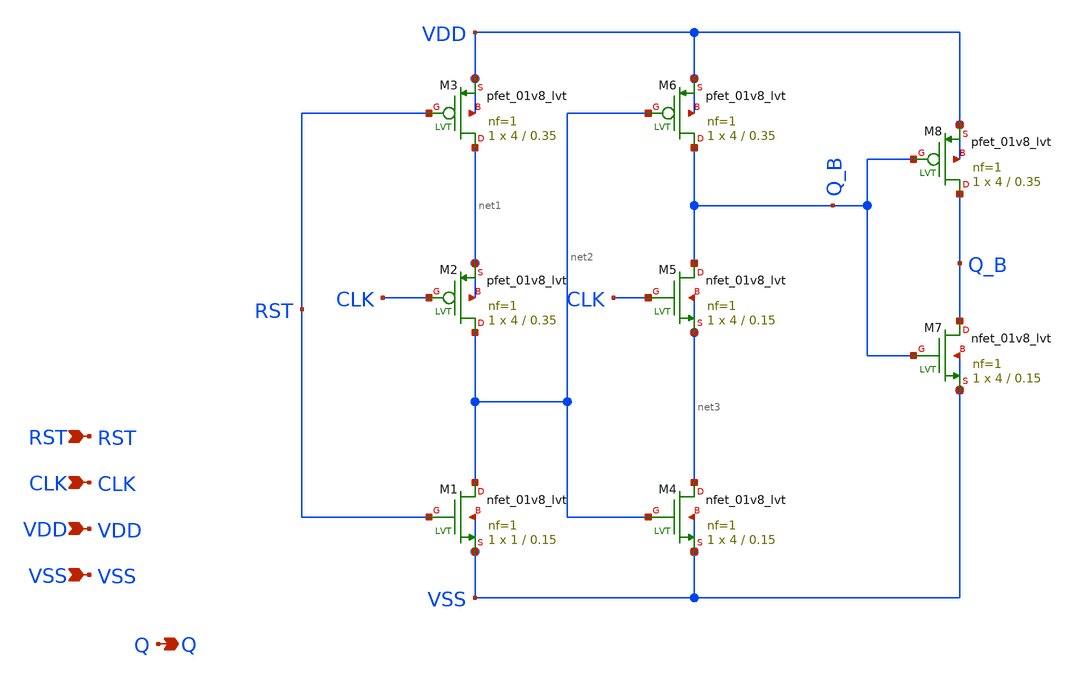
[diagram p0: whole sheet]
** sch_path: design/LELO_TSPC_FULL.sch
**.subckt LELO_TSPC_FULL RST CLK VDD VSS Q
*.ipin RST
*.ipin CLK
*.ipin VDD
*.ipin VSS
*.opin Q
XM1 net2 RST VSS VSS sky130_fd_pr__nfet_01v8_lvt L=0.15 W=1 nf=1 ad='int((1 + 1)/2) * 1 / 1 * 0.29' as='int((1 + 2)/2) * 1 / 1 * 0.29'
+ pd='2*int((1 + 1)/2) * (1 / 1 + 0.29)' ps='2*int((1 + 2)/2) * (1 / 1 + 0.29)' nrd='0.29 / 1 ' nrs='0.29 / 1 '
+ sa=0 sb=0 sd=0 mult=1 m=1
XM2 net2 CLK net1 net1 sky130_fd_pr__pfet_01v8_lvt L=0.35 W=4 nf=1 ad='int((1 + 1)/2) * 4 / 1 * 0.29'
+ as='int((1 + 2)/2) * 4 / 1 * 0.29' pd='2*int((1 + 1)/2) * (4 / 1 + 0.29)' ps='2*int((1 + 2)/2) * (4 / 1 + 0.29)'
+ nrd='0.29 / 4 ' nrs='0.29 / 4 ' sa=0 sb=0 sd=0 mult=1 m=1
XM3 net1 RST VDD VDD sky130_fd_pr__pfet_01v8_lvt L=0.35 W=4 nf=1 ad='int((1 + 1)/2) * 4 / 1 * 0.29' as='int((1 + 2)/2) * 4 / 1 * 0.29'
+ pd='2*int((1 + 1)/2) * (4 / 1 + 0.29)' ps='2*int((1 + 2)/2) * (4 / 1 + 0.29)' nrd='0.29 / 4 ' nrs='0.29 / 4 '
+ sa=0 sb=0 sd=0 mult=1 m=1
XM4 net3 net2 VSS VSS sky130_fd_pr__nfet_01v8_lvt L=0.15 W=4 nf=1 ad='int((1 + 1)/2) * 4 / 1 * 0.29'
+ as='int((1 + 2)/2) * 4 / 1 * 0.29' pd='2*int((1 + 1)/2) * (4 / 1 + 0.29)' ps='2*int((1 + 2)/2) * (4 / 1 + 0.29)'
+ nrd='0.29 / 4 ' nrs='0.29 / 4 ' sa=0 sb=0 sd=0 mult=1 m=1
XM5 Q_B CLK net3 net3 sky130_fd_pr__nfet_01v8_lvt L=0.15 W=4 nf=1 ad='int((1 + 1)/2) * 4 / 1 * 0.29'
+ as='int((1 + 2)/2) * 4 / 1 * 0.29' pd='2*int((1 + 1)/2) * (4 / 1 + 0.29)' ps='2*int((1 + 2)/2) * (4 / 1 + 0.29)'
+ nrd='0.29 / 4 ' nrs='0.29 / 4 ' sa=0 sb=0 sd=0 mult=1 m=1
XM6 Q_B net2 VDD VDD sky130_fd_pr__pfet_01v8_lvt L=0.35 W=4 nf=1 ad='int((1 + 1)/2) * 4 / 1 * 0.29' as='int((1 + 2)/2) * 4 / 1 * 0.29'
+ pd='2*int((1 + 1)/2) * (4 / 1 + 0.29)' ps='2*int((1 + 2)/2) * (4 / 1 + 0.29)' nrd='0.29 / 4 ' nrs='0.29 / 4 '
+ sa=0 sb=0 sd=0 mult=1 m=1
XM7 Q_B Q_B VSS VSS sky130_fd_pr__nfet_01v8_lvt L=0.15 W=4 nf=1 ad='int((1 + 1)/2) * 4 / 1 * 0.29' as='int((1 + 2)/2) * 4 / 1 * 0.29'
+ pd='2*int((1 + 1)/2) * (4 / 1 + 0.29)' ps='2*int((1 + 2)/2) * (4 / 1 + 0.29)' nrd='0.29 / 4 ' nrs='0.29 / 4 '
+ sa=0 sb=0 sd=0 mult=1 m=1
XM8 Q_B Q_B VDD VDD sky130_fd_pr__pfet_01v8_lvt L=0.35 W=4 nf=1 ad='int((1 + 1)/2) * 4 / 1 * 0.29' as='int((1 + 2)/2) * 4 / 1 * 0.29'
+ pd='2*int((1 + 1)/2) * (4 / 1 + 0.29)' ps='2*int((1 + 2)/2) * (4 / 1 + 0.29)' nrd='0.29 / 4 ' nrs='0.29 / 4 '
+ sa=0 sb=0 sd=0 mult=1 m=1
**.ends
.end
